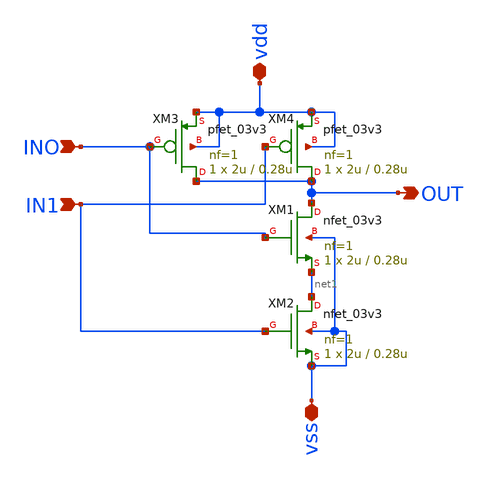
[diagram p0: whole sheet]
** sch_path: CAD6/DFF_Ray/NAND2.sch
**.subckt NAND2 INO IN1 vdd vss OUT
*.ipin INO
*.ipin IN1
*.iopin vdd
*.iopin vss
*.opin OUT
XM1 OUT INO net1 vss nfet_03v3 L=0.28u W=2u nf=1 ad='int((nf+1)/2) * W/nf * 0.18u' as='int((nf+2)/2) * W/nf * 0.18u'
+ pd='2*int((nf+1)/2) * (W/nf + 0.18u)' ps='2*int((nf+2)/2) * (W/nf + 0.18u)' nrd='0.18u / W' nrs='0.18u / W'
+ sa=0 sb=0 sd=0 m=1
XM2 net1 IN1 vss vss nfet_03v3 L=0.28u W=2u nf=1 ad='int((nf+1)/2) * W/nf * 0.18u' as='int((nf+2)/2) * W/nf * 0.18u'
+ pd='2*int((nf+1)/2) * (W/nf + 0.18u)' ps='2*int((nf+2)/2) * (W/nf + 0.18u)' nrd='0.18u / W' nrs='0.18u / W'
+ sa=0 sb=0 sd=0 m=1
XM3 OUT INO vdd vdd pfet_03v3 L=0.28u W=2u nf=1 ad='int((nf+1)/2) * W/nf * 0.18u' as='int((nf+2)/2) * W/nf * 0.18u'
+ pd='2*int((nf+1)/2) * (W/nf + 0.18u)' ps='2*int((nf+2)/2) * (W/nf + 0.18u)' nrd='0.18u / W' nrs='0.18u / W'
+ sa=0 sb=0 sd=0 m=1
XM4 OUT IN1 vdd vdd pfet_03v3 L=0.28u W=2u nf=1 ad='int((nf+1)/2) * W/nf * 0.18u' as='int((nf+2)/2) * W/nf * 0.18u'
+ pd='2*int((nf+1)/2) * (W/nf + 0.18u)' ps='2*int((nf+2)/2) * (W/nf + 0.18u)' nrd='0.18u / W' nrs='0.18u / W'
+ sa=0 sb=0 sd=0 m=1
**.ends
.end
